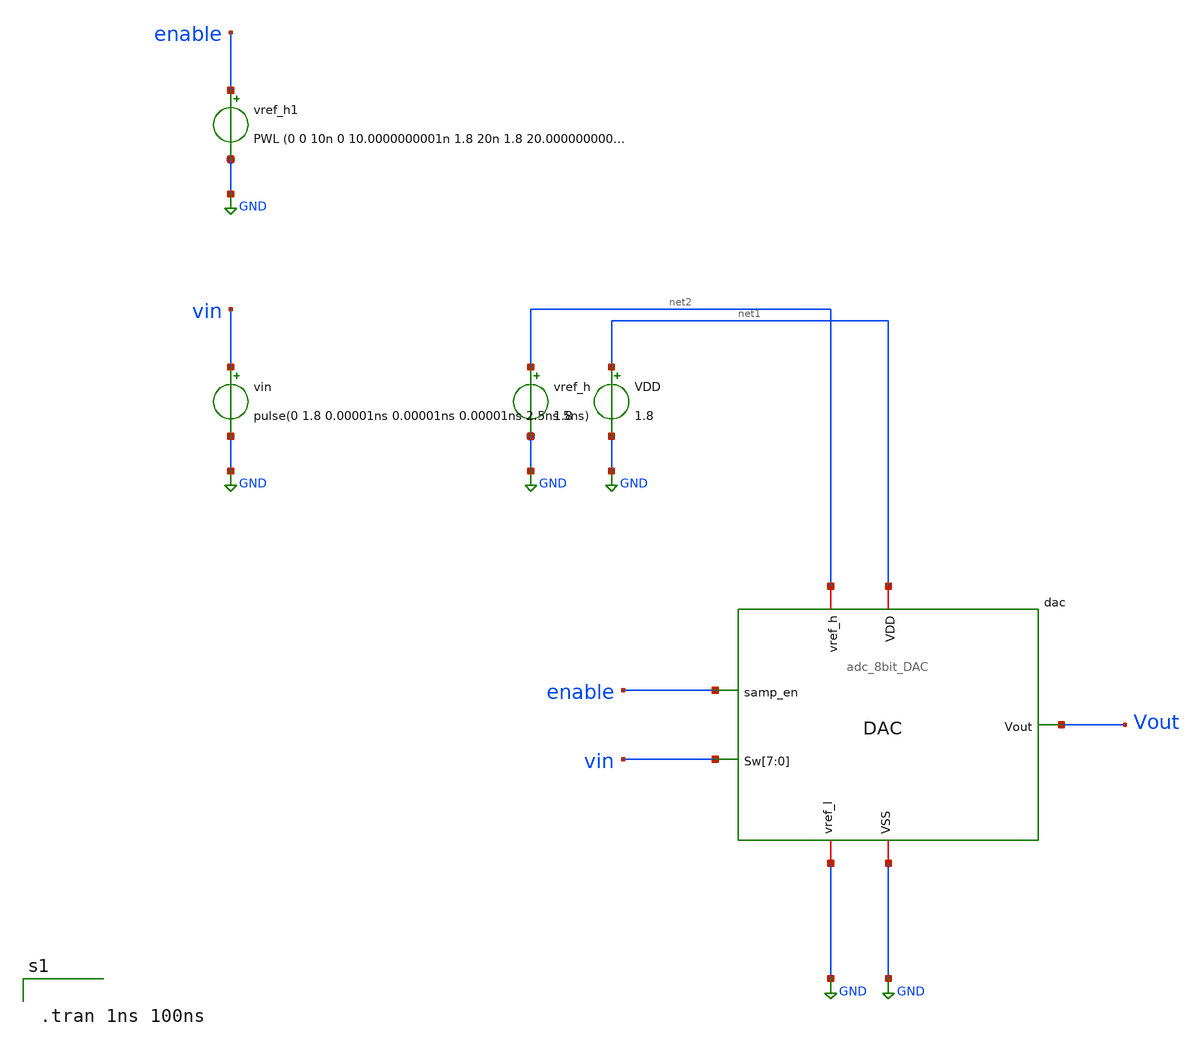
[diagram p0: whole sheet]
** sch_path: adc_8bit_DAC_tb.sch
**.subckt adc_8bit_DAC_tb
x1 Vout GND net1 net2 GND vin vin vin vin vin vin vin vin enable adc_8bit_DAC
VDD net1 GND 1.8
vref_h net2 GND 1.8
vin vin GND pulse(0 1.8 0.00001ns 0.00001ns 0.00001ns 2.5ns 5ns)
vref_h1 enable GND PWL (0 0 10n 0 10.0000000001n 1.8 20n 1.8 20.0000000000001n 0 1u 0)
**** begin user architecture code


.tran 1ns 100ns


** opencircuitdesign pdks install
.lib $::SKYWATER_MODELS/sky130.lib.spice tt
.include $::SKYWATER_STDCELLS/sky130_fd_sc_hd.spice

**** end user architecture code
**.ends

* expanding   symbol:  adc_8bit_DAC.sym # of pins=7
** sym_path: adc_8bit_DAC.sym
** sch_path: adc_8bit_DAC.sch
.subckt adc_8bit_DAC Vout VSS VDD vref_h vref_l Sw[7] Sw[6] Sw[5] Sw[4] Sw[3] Sw[2] Sw[1] Sw[0]
+ samp_en
*.ipin Sw[7],Sw[6],Sw[5],Sw[4],Sw[3],Sw[2],Sw[1],Sw[0]
*.ipin samp_en
*.iopin VSS
*.iopin VDD
*.iopin vref_h
*.iopin vref_l
*.opin Vout
XM23 net8 Sw[0] vref_l VSS sky130_fd_pr__nfet_01v8 L=0.28 W=2 nf=1 ad='int((nf+1)/2) * W/nf * 0.29' as='int((nf+2)/2) * W/nf * 0.29'
+ pd='2*int((nf+1)/2) * (W/nf + 0.29)' ps='2*int((nf+2)/2) * (W/nf + 0.29)' nrd='0.29 / W' nrs='0.29 / W'
+ sa=0 sb=0 sd=0 mult=1 m=1
XM21 net6 Sw[2] vref_l VSS sky130_fd_pr__nfet_01v8 L=0.24 W=1 nf=1 ad='int((nf+1)/2) * W/nf * 0.29' as='int((nf+2)/2) * W/nf * 0.29'
+ pd='2*int((nf+1)/2) * (W/nf + 0.29)' ps='2*int((nf+2)/2) * (W/nf + 0.29)' nrd='0.29 / W' nrs='0.29 / W'
+ sa=0 sb=0 sd=0 mult=1 m=1
XM24 net7 Sw[1] vref_l VSS sky130_fd_pr__nfet_01v8 L=0.24 W=1 nf=1 ad='int((nf+1)/2) * W/nf * 0.29' as='int((nf+2)/2) * W/nf * 0.29'
+ pd='2*int((nf+1)/2) * (W/nf + 0.29)' ps='2*int((nf+2)/2) * (W/nf + 0.29)' nrd='0.29 / W' nrs='0.29 / W'
+ sa=0 sb=0 sd=0 mult=1 m=1
XM25 net5 Sw[3] vref_l VSS sky130_fd_pr__nfet_01v8 L=0.24 W=1 nf=1 ad='int((nf+1)/2) * W/nf * 0.29' as='int((nf+2)/2) * W/nf * 0.29'
+ pd='2*int((nf+1)/2) * (W/nf + 0.29)' ps='2*int((nf+2)/2) * (W/nf + 0.29)' nrd='0.29 / W' nrs='0.29 / W'
+ sa=0 sb=0 sd=0 mult=1 m=1
XM26 Vout samp_en vref_l VSS sky130_fd_pr__nfet_01v8 L=0.3 W=10 nf=1 ad='int((nf+1)/2) * W/nf * 0.29'
+ as='int((nf+2)/2) * W/nf * 0.29' pd='2*int((nf+1)/2) * (W/nf + 0.29)' ps='2*int((nf+2)/2) * (W/nf + 0.29)'
+ nrd='0.29 / W' nrs='0.29 / W' sa=0 sb=0 sd=0 mult=1 m=1
XM27 net1 Sw[4] vref_l VSS sky130_fd_pr__nfet_01v8 L=0.24 W=1 nf=1 ad='int((nf+1)/2) * W/nf * 0.29' as='int((nf+2)/2) * W/nf * 0.29'
+ pd='2*int((nf+1)/2) * (W/nf + 0.29)' ps='2*int((nf+2)/2) * (W/nf + 0.29)' nrd='0.29 / W' nrs='0.29 / W'
+ sa=0 sb=0 sd=0 mult=1 m=1
XM28 net2 Sw[5] vref_l VSS sky130_fd_pr__nfet_01v8 L=0.24 W=2 nf=1 ad='int((nf+1)/2) * W/nf * 0.29' as='int((nf+2)/2) * W/nf * 0.29'
+ pd='2*int((nf+1)/2) * (W/nf + 0.29)' ps='2*int((nf+2)/2) * (W/nf + 0.29)' nrd='0.29 / W' nrs='0.29 / W'
+ sa=0 sb=0 sd=0 mult=1 m=1
XM29 net3 Sw[6] vref_l VSS sky130_fd_pr__nfet_01v8 L=0.24 W=2 nf=1 ad='int((nf+1)/2) * W/nf * 0.29' as='int((nf+2)/2) * W/nf * 0.29'
+ pd='2*int((nf+1)/2) * (W/nf + 0.29)' ps='2*int((nf+2)/2) * (W/nf + 0.29)' nrd='0.29 / W' nrs='0.29 / W'
+ sa=0 sb=0 sd=0 mult=1 m=1
XM30 net4 Sw[7] vref_l VSS sky130_fd_pr__nfet_01v8 L=0.24 W=2 nf=1 ad='int((nf+1)/2) * W/nf * 0.29' as='int((nf+2)/2) * W/nf * 0.29'
+ pd='2*int((nf+1)/2) * (W/nf + 0.29)' ps='2*int((nf+2)/2) * (W/nf + 0.29)' nrd='0.29 / W' nrs='0.29 / W'
+ sa=0 sb=0 sd=0 mult=1 m=1
XM9 vref_h Sw[0] net8 VDD sky130_fd_pr__pfet_01v8 L=0.28 W=2 nf=1 ad='int((nf+1)/2) * W/nf * 0.29' as='int((nf+2)/2) * W/nf * 0.29'
+ pd='2*int((nf+1)/2) * (W/nf + 0.29)' ps='2*int((nf+2)/2) * (W/nf + 0.29)' nrd='0.29 / W' nrs='0.29 / W'
+ sa=0 sb=0 sd=0 mult=1 m=1
XM1 vref_h Sw[1] net7 VDD sky130_fd_pr__pfet_01v8 L=0.24 W=1 nf=1 ad='int((nf+1)/2) * W/nf * 0.29' as='int((nf+2)/2) * W/nf * 0.29'
+ pd='2*int((nf+1)/2) * (W/nf + 0.29)' ps='2*int((nf+2)/2) * (W/nf + 0.29)' nrd='0.29 / W' nrs='0.29 / W'
+ sa=0 sb=0 sd=0 mult=1 m=1
XM2 vref_h Sw[2] net6 VDD sky130_fd_pr__pfet_01v8 L=0.24 W=1 nf=1 ad='int((nf+1)/2) * W/nf * 0.29' as='int((nf+2)/2) * W/nf * 0.29'
+ pd='2*int((nf+1)/2) * (W/nf + 0.29)' ps='2*int((nf+2)/2) * (W/nf + 0.29)' nrd='0.29 / W' nrs='0.29 / W'
+ sa=0 sb=0 sd=0 mult=1 m=1
XM3 vref_h Sw[3] net5 VDD sky130_fd_pr__pfet_01v8 L=0.24 W=1 nf=1 ad='int((nf+1)/2) * W/nf * 0.29' as='int((nf+2)/2) * W/nf * 0.29'
+ pd='2*int((nf+1)/2) * (W/nf + 0.29)' ps='2*int((nf+2)/2) * (W/nf + 0.29)' nrd='0.29 / W' nrs='0.29 / W'
+ sa=0 sb=0 sd=0 mult=1 m=1
XM4 vref_h Sw[4] net1 VDD sky130_fd_pr__pfet_01v8 L=0.24 W=1 nf=1 ad='int((nf+1)/2) * W/nf * 0.29' as='int((nf+2)/2) * W/nf * 0.29'
+ pd='2*int((nf+1)/2) * (W/nf + 0.29)' ps='2*int((nf+2)/2) * (W/nf + 0.29)' nrd='0.29 / W' nrs='0.29 / W'
+ sa=0 sb=0 sd=0 mult=1 m=1
XM5 vref_h Sw[5] net2 VDD sky130_fd_pr__pfet_01v8 L=0.24 W=2 nf=1 ad='int((nf+1)/2) * W/nf * 0.29' as='int((nf+2)/2) * W/nf * 0.29'
+ pd='2*int((nf+1)/2) * (W/nf + 0.29)' ps='2*int((nf+2)/2) * (W/nf + 0.29)' nrd='0.29 / W' nrs='0.29 / W'
+ sa=0 sb=0 sd=0 mult=1 m=1
XM6 vref_h Sw[6] net3 VDD sky130_fd_pr__pfet_01v8 L=0.24 W=2 nf=1 ad='int((nf+1)/2) * W/nf * 0.29' as='int((nf+2)/2) * W/nf * 0.29'
+ pd='2*int((nf+1)/2) * (W/nf + 0.29)' ps='2*int((nf+2)/2) * (W/nf + 0.29)' nrd='0.29 / W' nrs='0.29 / W'
+ sa=0 sb=0 sd=0 mult=1 m=1
XM7 vref_h Sw[7] net4 VDD sky130_fd_pr__pfet_01v8 L=0.24 W=2 nf=1 ad='int((nf+1)/2) * W/nf * 0.29' as='int((nf+2)/2) * W/nf * 0.29'
+ pd='2*int((nf+1)/2) * (W/nf + 0.29)' ps='2*int((nf+2)/2) * (W/nf + 0.29)' nrd='0.29 / W' nrs='0.29 / W'
+ sa=0 sb=0 sd=0 mult=1 m=1
XC3 Vout net7 sky130_fd_pr__cap_mim_m3_1 W=1 L=1 MF=1 m=1
XC4 Vout net6 sky130_fd_pr__cap_mim_m3_1 W=2 L=1.1 MF=1 m=1
XC5 Vout net5 sky130_fd_pr__cap_mim_m3_1 W=2.5 L=2 MF=1 m=1
XC6 Vout net1 sky130_fd_pr__cap_mim_m3_1 W=3.5 L=3 MF=1 m=1
XC7 Vout net2 sky130_fd_pr__cap_mim_m3_1 W=5 L=4.3 MF=1 m=1
XC10 net9 vref_l sky130_fd_pr__cap_mim_m3_1 W=3 L=3 MF=1 m=1
XC8 Vout net3 sky130_fd_pr__cap_mim_m3_1 W=7 L=6.3 MF=1 m=1
XC9 Vout net4 sky130_fd_pr__cap_mim_m3_1 W=10 L=9 MF=1 m=1
XC11 Vout net9 sky130_fd_pr__cap_mim_m3_1 W=3 L=3 MF=1 m=1
XC2 Vout net10 sky130_fd_pr__cap_mim_m3_1 W=2.6 L=2.6 MF=1 m=1
XC1 net10 net8 sky130_fd_pr__cap_mim_m3_1 W=3 L=3 MF=1 m=1
.ends

.GLOBAL GND
.end
